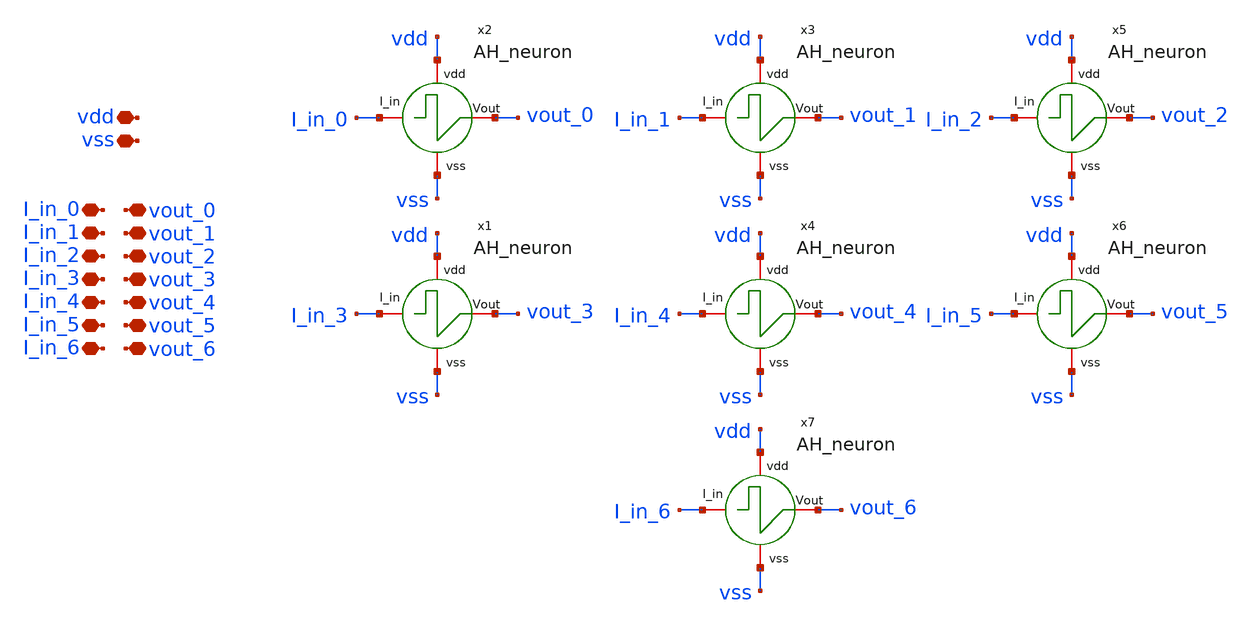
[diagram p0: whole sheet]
** sch_path: designs/libs/core_AH_neuron_arr/AH_neuron_arr.sch
**.subckt AH_neuron_arr vdd vss I_in_0 vout_0 I_in_6 vout_6 I_in_1 vout_1 I_in_2 vout_2 I_in_3
*+ vout_3 I_in_4 vout_4 I_in_5 vout_5
*.iopin vdd
*.iopin vss
*.iopin I_in_0
*.iopin vout_0
*.iopin I_in_6
*.iopin vout_6
*.iopin I_in_1
*.iopin vout_1
*.iopin I_in_2
*.iopin vout_2
*.iopin I_in_3
*.iopin vout_3
*.iopin I_in_4
*.iopin vout_4
*.iopin I_in_5
*.iopin vout_5
x1 vdd I_in_3 vout_3 vss AH_neuron
x2 vdd I_in_0 vout_0 vss AH_neuron
x3 vdd I_in_1 vout_1 vss AH_neuron
x4 vdd I_in_4 vout_4 vss AH_neuron
x5 vdd I_in_2 vout_2 vss AH_neuron
x6 vdd I_in_5 vout_5 vss AH_neuron
x7 vdd I_in_6 vout_6 vss AH_neuron
**.ends

* expanding   symbol:  designs/libs/core_AH_neuron/AH_neuron.sym # of pins=4
** sym_path: designs/libs/core_AH_neuron/AH_neuron.sym
** sch_path: designs/libs/core_AH_neuron/AH_neuron.sch
.subckt AH_neuron vdd Current_in Vout vss
*.iopin vdd
*.iopin vss
*.iopin Current_in
*.iopin Vout
XM5 Vout net1 vdd vdd pfet_03v3 L=0.28u W=0.42u nf=1 ad='int((nf+1)/2) * W/nf * 0.18u' as='int((nf+2)/2) * W/nf * 0.18u'
+ pd='2*int((nf+1)/2) * (W/nf + 0.18u)' ps='2*int((nf+2)/2) * (W/nf + 0.18u)' nrd='0.18u / W' nrs='0.18u / W'
+ sa=0 sb=0 sd=0 m=1
XM1 net1 Current_in vdd vdd pfet_03v3 L=0.56u W=0.44u nf=1 ad='int((nf+1)/2) * W/nf * 0.18u' as='int((nf+2)/2) * W/nf * 0.18u'
+ pd='2*int((nf+1)/2) * (W/nf + 0.18u)' ps='2*int((nf+2)/2) * (W/nf + 0.18u)' nrd='0.18u / W' nrs='0.18u / W'
+ sa=0 sb=0 sd=0 m=1
XM2 Vout net1 vss vss nfet_03v3 L=0.28u W=0.42u nf=1 ad='int((nf+1)/2) * W/nf * 0.18u' as='int((nf+2)/2) * W/nf * 0.18u'
+ pd='2*int((nf+1)/2) * (W/nf + 0.18u)' ps='2*int((nf+2)/2) * (W/nf + 0.18u)' nrd='0.18u / W' nrs='0.18u / W'
+ sa=0 sb=0 sd=0 m=1
XM3 net1 Current_in vss vss nfet_03v3 L=0.56u W=0.44u nf=1 ad='int((nf+1)/2) * W/nf * 0.18u' as='int((nf+2)/2) * W/nf * 0.18u'
+ pd='2*int((nf+1)/2) * (W/nf + 0.18u)' ps='2*int((nf+2)/2) * (W/nf + 0.18u)' nrd='0.18u / W' nrs='0.18u / W'
+ sa=0 sb=0 sd=0 m=1
XM4 Current_in vgl vss vss nfet_03v3 L=4.2u W=0.42u nf=1 ad='int((nf+1)/2) * W/nf * 0.18u' as='int((nf+2)/2) * W/nf * 0.18u'
+ pd='2*int((nf+1)/2) * (W/nf + 0.18u)' ps='2*int((nf+2)/2) * (W/nf + 0.18u)' nrd='0.18u / W' nrs='0.18u / W'
+ sa=0 sb=0 sd=0 m=1
XC1 Current_in Vout cap_mim_1f0fF c_width=1e-6 c_length=1e-6 m=25
XC2 Vout vgl cap_mim_1f0fF c_width=1e-6 c_length=1e-6 m=1
.ends

.end
